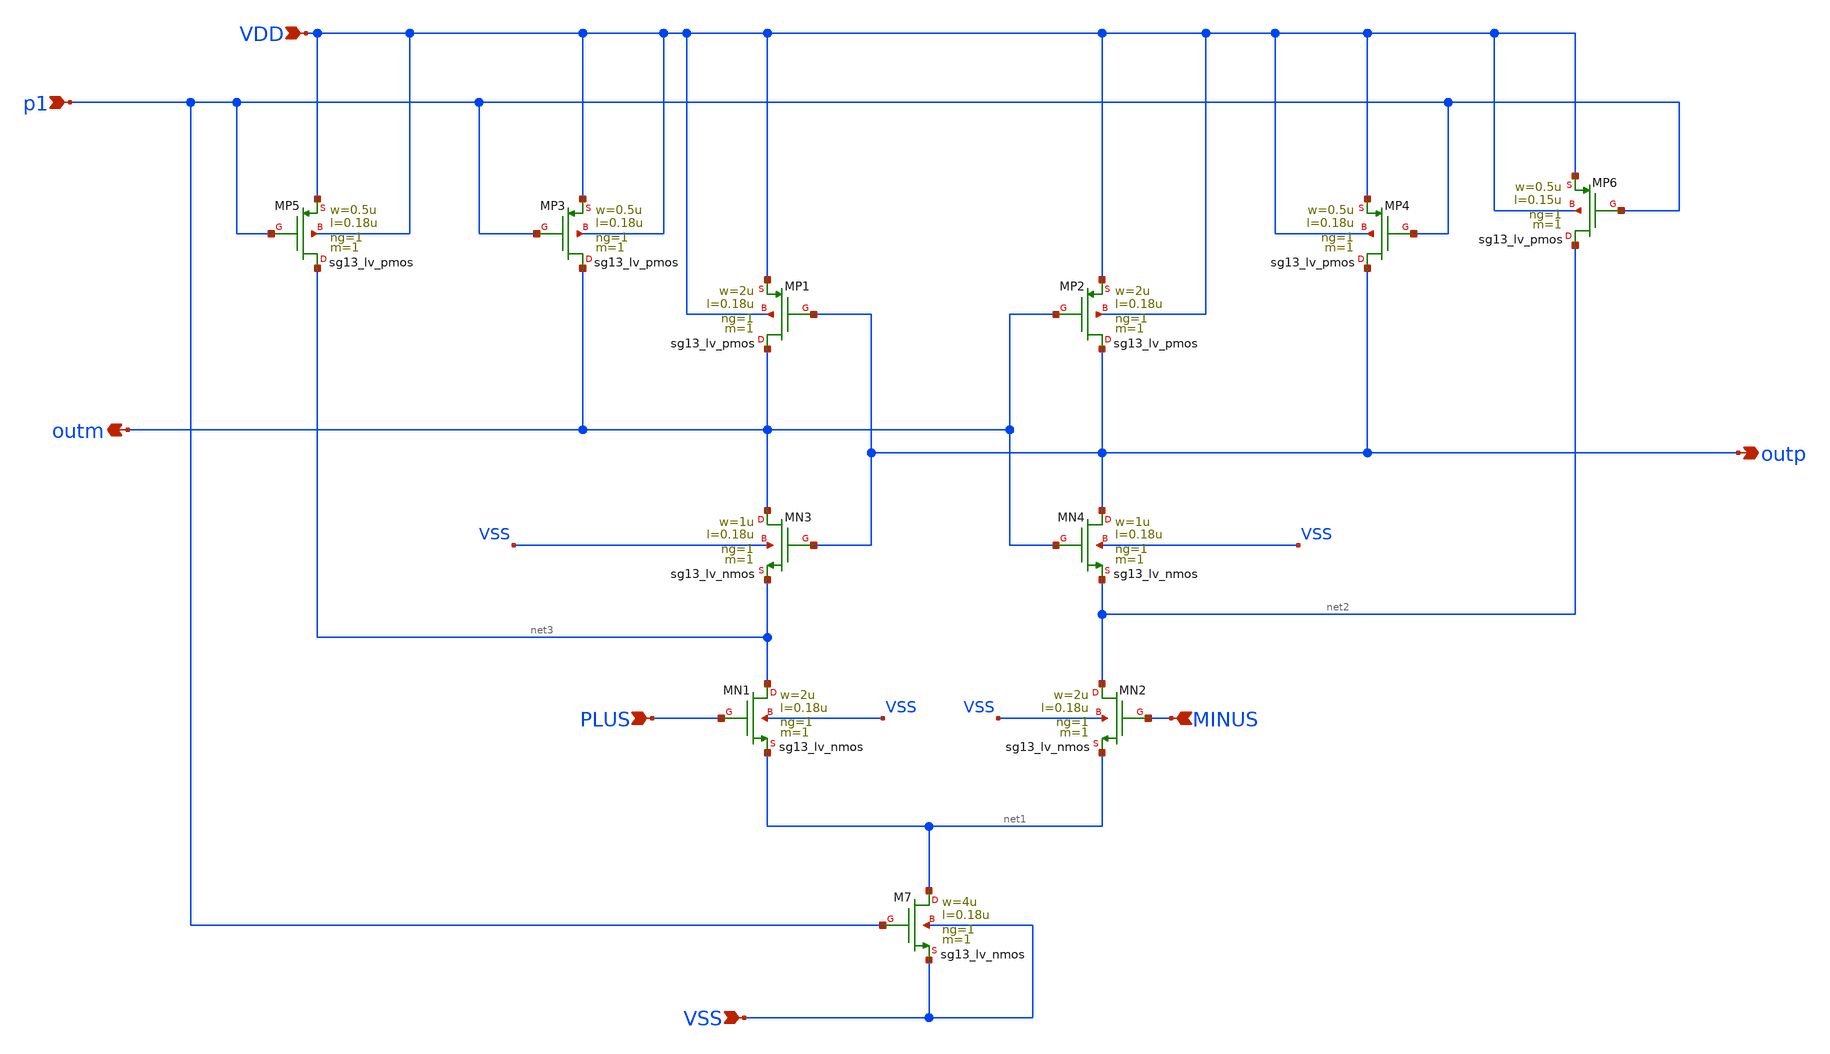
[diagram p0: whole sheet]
** sch_path: DSM/Sneha/Comp_Test-2.sch
**.subckt Comp_Test-2 PLUS MINUS VDD VSS p1 outp outm
*.ipin PLUS
*.ipin MINUS
*.ipin VDD
*.ipin VSS
*.ipin p1
*.opin outp
*.opin outm
XMN3 outm outp net3 VSS sg13_lv_nmos w=1u l=0.18u ng=1 m=1 mm_ok=1
XMP5 net3 p1 VDD VDD sg13_lv_pmos w=0.5u l=0.18u ng=1 m=1 mm_ok=1
XMP3 outm p1 VDD VDD sg13_lv_pmos w=0.5u l=0.18u ng=1 m=1 mm_ok=1
XMP1 outm outp VDD VDD sg13_lv_pmos w=2u l=0.18u ng=1 m=1 mm_ok=1
XMP2 outp outm VDD VDD sg13_lv_pmos w=2u l=0.18u ng=1 m=1 mm_ok=1
XMP4 outp p1 VDD VDD sg13_lv_pmos w=0.5u l=0.18u ng=1 m=1 mm_ok=1
XMP6 net2 p1 VDD VDD sg13_lv_pmos w=0.5u l=0.15u ng=1 m=1 mm_ok=1
XMN4 outp outm net2 VSS sg13_lv_nmos w=1u l=0.18u ng=1 m=1 mm_ok=1
XMN1 net3 PLUS net1 VSS sg13_lv_nmos w=2u l=0.18u ng=1 m=1 mm_ok=1
XMN2 net2 MINUS net1 VSS sg13_lv_nmos w=2u l=0.18u ng=1 m=1 mm_ok=1
XM7 net1 p1 VSS VSS sg13_lv_nmos w=4u l=0.18u ng=1 m=1 mm_ok=1
**.ends
.end
